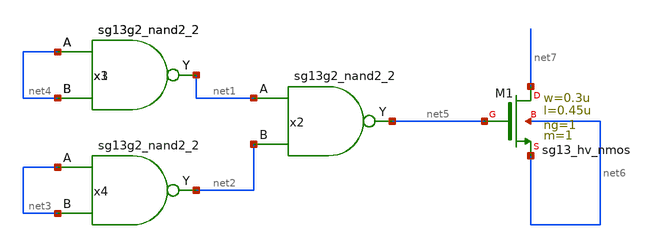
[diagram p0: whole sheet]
** sch_path: readout_circuit/analog/nand_nand_CS.sch
**.subckt nand_nand_CS
x3 net1 net4 net4 VDD VSS sg13g2_nand2_2
x1 net1 net4 net4 VDD VSS sg13g2_nand2_2
x2 net5 net1 net2 VDD VSS sg13g2_nand2_2
x4 net2 net3 net3 VDD VSS sg13g2_nand2_2
XM1 net7 net5 net6 net6 sg13_hv_nmos w=0.3u l=0.45u ng=1 m=1 mm_ok=1
**.ends

* expanding   symbol:  sg13g2_stdcells/sg13g2_nand2_2.sym # of pins=3
** sym_path: sg13g2_stdcells/sg13g2_nand2_2.sym
** sch_path: sg13g2_stdcells/sg13g2_nand2_2.sch
.subckt sg13g2_nand2_2 Y A B VDD VSS
*.iopin VDD
*.iopin VSS
*.opin Y
*.ipin B
*.ipin A
XM1 Y A net1 VSS sg13_lv_nmos w=1.44u l=130.00n ng=2 m=1 mm_ok=1
XM2 net1 B VSS VSS sg13_lv_nmos w=1.44u l=130.00n ng=2 m=1 mm_ok=1
XM3 Y A VDD VDD sg13_lv_pmos w=2.24u l=130.00n ng=2 m=1 mm_ok=1
XM4 Y B VDD VDD sg13_lv_pmos w=2.24u l=130.00n ng=2 m=1 mm_ok=1
.ends

.end
